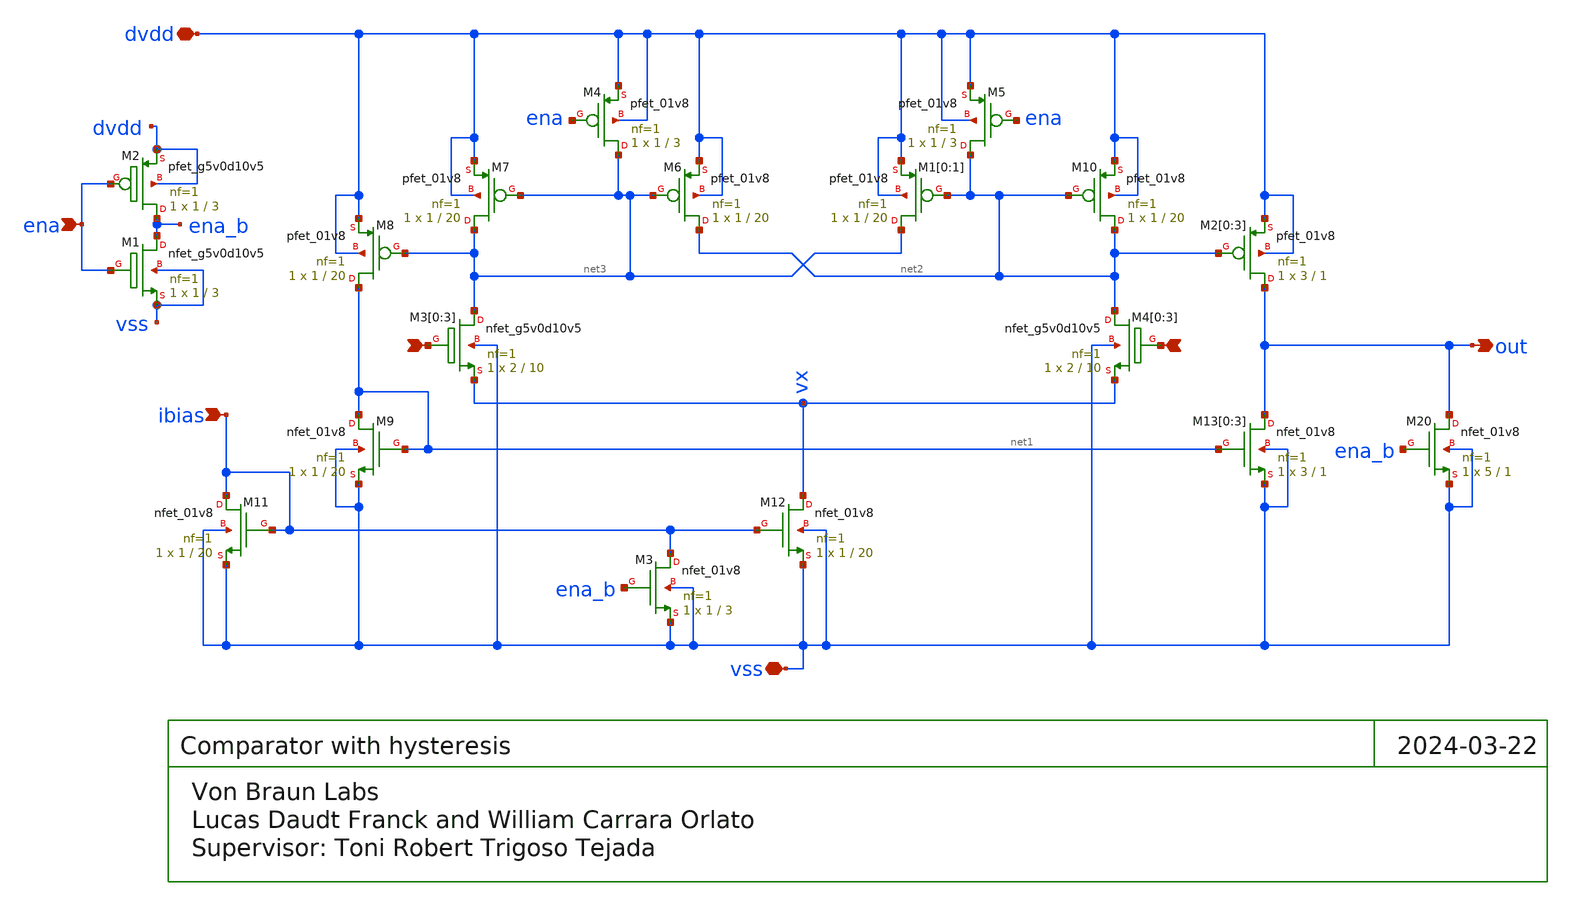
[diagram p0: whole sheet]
** sch_path: xschem/comp_hyst.sch
**.subckt comp_hyst dvdd - + out ibias ena vss
*.iopin dvdd
*.ipin -
*.ipin +
*.opin out
*.ipin ibias
*.ipin ena
*.iopin vss
XM4 net3 ena dvdd dvdd sky130_fd_pr__pfet_01v8 L=3 W=1 nf=1 ad='int((nf+1)/2) * W/nf * 0.29' as='int((nf+2)/2) * W/nf * 0.29'
+ pd='2*int((nf+1)/2) * (W/nf + 0.29)' ps='2*int((nf+2)/2) * (W/nf + 0.29)' nrd='0.29 / W' nrs='0.29 / W'
+ sa=0 sb=0 sd=0 mult=1 m=1
XM5 net2 ena dvdd dvdd sky130_fd_pr__pfet_01v8 L=3 W=1 nf=1 ad='int((nf+1)/2) * W/nf * 0.29' as='int((nf+2)/2) * W/nf * 0.29'
+ pd='2*int((nf+1)/2) * (W/nf + 0.29)' ps='2*int((nf+2)/2) * (W/nf + 0.29)' nrd='0.29 / W' nrs='0.29 / W'
+ sa=0 sb=0 sd=0 mult=1 m=1
XM6 net2 net3 dvdd dvdd sky130_fd_pr__pfet_01v8 L=20 W=1 nf=1 ad='int((nf+1)/2) * W/nf * 0.29' as='int((nf+2)/2) * W/nf * 0.29'
+ pd='2*int((nf+1)/2) * (W/nf + 0.29)' ps='2*int((nf+2)/2) * (W/nf + 0.29)' nrd='0.29 / W' nrs='0.29 / W'
+ sa=0 sb=0 sd=0 mult=1 m=1
XM7 net3 net3 dvdd dvdd sky130_fd_pr__pfet_01v8 L=20 W=1 nf=1 ad='int((nf+1)/2) * W/nf * 0.29' as='int((nf+2)/2) * W/nf * 0.29'
+ pd='2*int((nf+1)/2) * (W/nf + 0.29)' ps='2*int((nf+2)/2) * (W/nf + 0.29)' nrd='0.29 / W' nrs='0.29 / W'
+ sa=0 sb=0 sd=0 mult=1 m=1
XM8 net1 net3 dvdd dvdd sky130_fd_pr__pfet_01v8 L=20 W=1 nf=1 ad='int((nf+1)/2) * W/nf * 0.29' as='int((nf+2)/2) * W/nf * 0.29'
+ pd='2*int((nf+1)/2) * (W/nf + 0.29)' ps='2*int((nf+2)/2) * (W/nf + 0.29)' nrd='0.29 / W' nrs='0.29 / W'
+ sa=0 sb=0 sd=0 mult=1 m=1
XM10 net2 net2 dvdd dvdd sky130_fd_pr__pfet_01v8 L=20 W=1 nf=1 ad='int((nf+1)/2) * W/nf * 0.29' as='int((nf+2)/2) * W/nf * 0.29'
+ pd='2*int((nf+1)/2) * (W/nf + 0.29)' ps='2*int((nf+2)/2) * (W/nf + 0.29)' nrd='0.29 / W' nrs='0.29 / W'
+ sa=0 sb=0 sd=0 mult=1 m=1
XM11 ibias ibias vss vss sky130_fd_pr__nfet_01v8 L=20 W=1 nf=1 ad='int((nf+1)/2) * W/nf * 0.29' as='int((nf+2)/2) * W/nf * 0.29'
+ pd='2*int((nf+1)/2) * (W/nf + 0.29)' ps='2*int((nf+2)/2) * (W/nf + 0.29)' nrd='0.29 / W' nrs='0.29 / W'
+ sa=0 sb=0 sd=0 mult=1 m=1
XM12 vx ibias vss vss sky130_fd_pr__nfet_01v8 L=20 W=1 nf=1 ad='int((nf+1)/2) * W/nf * 0.29' as='int((nf+2)/2) * W/nf * 0.29'
+ pd='2*int((nf+1)/2) * (W/nf + 0.29)' ps='2*int((nf+2)/2) * (W/nf + 0.29)' nrd='0.29 / W' nrs='0.29 / W'
+ sa=0 sb=0 sd=0 mult=1 m=1
XM2[0] out net2 dvdd dvdd sky130_fd_pr__pfet_01v8 L=1 W=3 nf=1 ad='int((nf+1)/2) * W/nf * 0.29' as='int((nf+2)/2) * W/nf * 0.29'
+ pd='2*int((nf+1)/2) * (W/nf + 0.29)' ps='2*int((nf+2)/2) * (W/nf + 0.29)' nrd='0.29 / W' nrs='0.29 / W'
+ sa=0 sb=0 sd=0 mult=1 m=1
XM2[1] out net2 dvdd dvdd sky130_fd_pr__pfet_01v8 L=1 W=3 nf=1 ad='int((nf+1)/2) * W/nf * 0.29' as='int((nf+2)/2) * W/nf * 0.29'
+ pd='2*int((nf+1)/2) * (W/nf + 0.29)' ps='2*int((nf+2)/2) * (W/nf + 0.29)' nrd='0.29 / W' nrs='0.29 / W'
+ sa=0 sb=0 sd=0 mult=1 m=1
XM2[2] out net2 dvdd dvdd sky130_fd_pr__pfet_01v8 L=1 W=3 nf=1 ad='int((nf+1)/2) * W/nf * 0.29' as='int((nf+2)/2) * W/nf * 0.29'
+ pd='2*int((nf+1)/2) * (W/nf + 0.29)' ps='2*int((nf+2)/2) * (W/nf + 0.29)' nrd='0.29 / W' nrs='0.29 / W'
+ sa=0 sb=0 sd=0 mult=1 m=1
XM2[3] out net2 dvdd dvdd sky130_fd_pr__pfet_01v8 L=1 W=3 nf=1 ad='int((nf+1)/2) * W/nf * 0.29' as='int((nf+2)/2) * W/nf * 0.29'
+ pd='2*int((nf+1)/2) * (W/nf + 0.29)' ps='2*int((nf+2)/2) * (W/nf + 0.29)' nrd='0.29 / W' nrs='0.29 / W'
+ sa=0 sb=0 sd=0 mult=1 m=1
XM13[0] out net1 vss vss sky130_fd_pr__nfet_01v8 L=1 W=3 nf=1 ad='int((nf+1)/2) * W/nf * 0.29' as='int((nf+2)/2) * W/nf * 0.29'
+ pd='2*int((nf+1)/2) * (W/nf + 0.29)' ps='2*int((nf+2)/2) * (W/nf + 0.29)' nrd='0.29 / W' nrs='0.29 / W'
+ sa=0 sb=0 sd=0 mult=1 m=1
XM13[1] out net1 vss vss sky130_fd_pr__nfet_01v8 L=1 W=3 nf=1 ad='int((nf+1)/2) * W/nf * 0.29' as='int((nf+2)/2) * W/nf * 0.29'
+ pd='2*int((nf+1)/2) * (W/nf + 0.29)' ps='2*int((nf+2)/2) * (W/nf + 0.29)' nrd='0.29 / W' nrs='0.29 / W'
+ sa=0 sb=0 sd=0 mult=1 m=1
XM13[2] out net1 vss vss sky130_fd_pr__nfet_01v8 L=1 W=3 nf=1 ad='int((nf+1)/2) * W/nf * 0.29' as='int((nf+2)/2) * W/nf * 0.29'
+ pd='2*int((nf+1)/2) * (W/nf + 0.29)' ps='2*int((nf+2)/2) * (W/nf + 0.29)' nrd='0.29 / W' nrs='0.29 / W'
+ sa=0 sb=0 sd=0 mult=1 m=1
XM13[3] out net1 vss vss sky130_fd_pr__nfet_01v8 L=1 W=3 nf=1 ad='int((nf+1)/2) * W/nf * 0.29' as='int((nf+2)/2) * W/nf * 0.29'
+ pd='2*int((nf+1)/2) * (W/nf + 0.29)' ps='2*int((nf+2)/2) * (W/nf + 0.29)' nrd='0.29 / W' nrs='0.29 / W'
+ sa=0 sb=0 sd=0 mult=1 m=1
XM20 out ena_b vss vss sky130_fd_pr__nfet_01v8 L=1 W=5 nf=1 ad='int((nf+1)/2) * W/nf * 0.29' as='int((nf+2)/2) * W/nf * 0.29'
+ pd='2*int((nf+1)/2) * (W/nf + 0.29)' ps='2*int((nf+2)/2) * (W/nf + 0.29)' nrd='0.29 / W' nrs='0.29 / W'
+ sa=0 sb=0 sd=0 mult=1 m=1
XM3[0] net3 - vx vss sky130_fd_pr__nfet_g5v0d10v5 L=10 W=2 nf=1 ad='int((nf+1)/2) * W/nf * 0.29' as='int((nf+2)/2) * W/nf * 0.29'
+ pd='2*int((nf+1)/2) * (W/nf + 0.29)' ps='2*int((nf+2)/2) * (W/nf + 0.29)' nrd='0.29 / W' nrs='0.29 / W'
+ sa=0 sb=0 sd=0 mult=1 m=1
XM3[1] net3 - vx vss sky130_fd_pr__nfet_g5v0d10v5 L=10 W=2 nf=1 ad='int((nf+1)/2) * W/nf * 0.29' as='int((nf+2)/2) * W/nf * 0.29'
+ pd='2*int((nf+1)/2) * (W/nf + 0.29)' ps='2*int((nf+2)/2) * (W/nf + 0.29)' nrd='0.29 / W' nrs='0.29 / W'
+ sa=0 sb=0 sd=0 mult=1 m=1
XM3[2] net3 - vx vss sky130_fd_pr__nfet_g5v0d10v5 L=10 W=2 nf=1 ad='int((nf+1)/2) * W/nf * 0.29' as='int((nf+2)/2) * W/nf * 0.29'
+ pd='2*int((nf+1)/2) * (W/nf + 0.29)' ps='2*int((nf+2)/2) * (W/nf + 0.29)' nrd='0.29 / W' nrs='0.29 / W'
+ sa=0 sb=0 sd=0 mult=1 m=1
XM3[3] net3 - vx vss sky130_fd_pr__nfet_g5v0d10v5 L=10 W=2 nf=1 ad='int((nf+1)/2) * W/nf * 0.29' as='int((nf+2)/2) * W/nf * 0.29'
+ pd='2*int((nf+1)/2) * (W/nf + 0.29)' ps='2*int((nf+2)/2) * (W/nf + 0.29)' nrd='0.29 / W' nrs='0.29 / W'
+ sa=0 sb=0 sd=0 mult=1 m=1
XM4[0] net2 + vx vss sky130_fd_pr__nfet_g5v0d10v5 L=10 W=2 nf=1 ad='int((nf+1)/2) * W/nf * 0.29' as='int((nf+2)/2) * W/nf * 0.29'
+ pd='2*int((nf+1)/2) * (W/nf + 0.29)' ps='2*int((nf+2)/2) * (W/nf + 0.29)' nrd='0.29 / W' nrs='0.29 / W'
+ sa=0 sb=0 sd=0 mult=1 m=1
XM4[1] net2 + vx vss sky130_fd_pr__nfet_g5v0d10v5 L=10 W=2 nf=1 ad='int((nf+1)/2) * W/nf * 0.29' as='int((nf+2)/2) * W/nf * 0.29'
+ pd='2*int((nf+1)/2) * (W/nf + 0.29)' ps='2*int((nf+2)/2) * (W/nf + 0.29)' nrd='0.29 / W' nrs='0.29 / W'
+ sa=0 sb=0 sd=0 mult=1 m=1
XM4[2] net2 + vx vss sky130_fd_pr__nfet_g5v0d10v5 L=10 W=2 nf=1 ad='int((nf+1)/2) * W/nf * 0.29' as='int((nf+2)/2) * W/nf * 0.29'
+ pd='2*int((nf+1)/2) * (W/nf + 0.29)' ps='2*int((nf+2)/2) * (W/nf + 0.29)' nrd='0.29 / W' nrs='0.29 / W'
+ sa=0 sb=0 sd=0 mult=1 m=1
XM4[3] net2 + vx vss sky130_fd_pr__nfet_g5v0d10v5 L=10 W=2 nf=1 ad='int((nf+1)/2) * W/nf * 0.29' as='int((nf+2)/2) * W/nf * 0.29'
+ pd='2*int((nf+1)/2) * (W/nf + 0.29)' ps='2*int((nf+2)/2) * (W/nf + 0.29)' nrd='0.29 / W' nrs='0.29 / W'
+ sa=0 sb=0 sd=0 mult=1 m=1
XM3 ibias ena_b vss vss sky130_fd_pr__nfet_01v8 L=3 W=1 nf=1 ad='int((nf+1)/2) * W/nf * 0.29' as='int((nf+2)/2) * W/nf * 0.29'
+ pd='2*int((nf+1)/2) * (W/nf + 0.29)' ps='2*int((nf+2)/2) * (W/nf + 0.29)' nrd='0.29 / W' nrs='0.29 / W'
+ sa=0 sb=0 sd=0 mult=1 m=1
XM1[0] net3 net2 dvdd dvdd sky130_fd_pr__pfet_01v8 L=20 W=1 nf=1 ad='int((nf+1)/2) * W/nf * 0.29' as='int((nf+2)/2) * W/nf * 0.29'
+ pd='2*int((nf+1)/2) * (W/nf + 0.29)' ps='2*int((nf+2)/2) * (W/nf + 0.29)' nrd='0.29 / W' nrs='0.29 / W'
+ sa=0 sb=0 sd=0 mult=1 m=1
XM1[1] net3 net2 dvdd dvdd sky130_fd_pr__pfet_01v8 L=20 W=1 nf=1 ad='int((nf+1)/2) * W/nf * 0.29' as='int((nf+2)/2) * W/nf * 0.29'
+ pd='2*int((nf+1)/2) * (W/nf + 0.29)' ps='2*int((nf+2)/2) * (W/nf + 0.29)' nrd='0.29 / W' nrs='0.29 / W'
+ sa=0 sb=0 sd=0 mult=1 m=1
XM1 ena_b ena vss vss sky130_fd_pr__nfet_g5v0d10v5 L=3 W=1 nf=1 ad='int((nf+1)/2) * W/nf * 0.29' as='int((nf+2)/2) * W/nf * 0.29'
+ pd='2*int((nf+1)/2) * (W/nf + 0.29)' ps='2*int((nf+2)/2) * (W/nf + 0.29)' nrd='0.29 / W' nrs='0.29 / W'
+ sa=0 sb=0 sd=0 mult=1 m=1
XM2 ena_b ena dvdd dvdd sky130_fd_pr__pfet_g5v0d10v5 L=3 W=1 nf=1 ad='int((nf+1)/2) * W/nf * 0.29' as='int((nf+2)/2) * W/nf * 0.29'
+ pd='2*int((nf+1)/2) * (W/nf + 0.29)' ps='2*int((nf+2)/2) * (W/nf + 0.29)' nrd='0.29 / W' nrs='0.29 / W'
+ sa=0 sb=0 sd=0 mult=1 m=1
XM9 net1 net1 vss vss sky130_fd_pr__nfet_01v8 L=20 W=1 nf=1 ad='int((nf+1)/2) * W/nf * 0.29' as='int((nf+2)/2) * W/nf * 0.29'
+ pd='2*int((nf+1)/2) * (W/nf + 0.29)' ps='2*int((nf+2)/2) * (W/nf + 0.29)' nrd='0.29 / W' nrs='0.29 / W'
+ sa=0 sb=0 sd=0 mult=1 m=1
**.ends
.end
